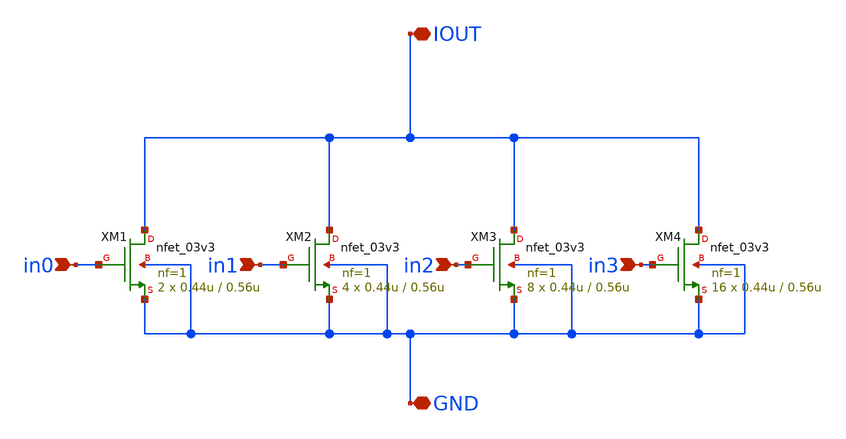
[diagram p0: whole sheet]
** sch_path: xschem/current_dac.sch
**.subckt current_dac in0 IOUT GND in1 in2 in3
*.ipin in0
*.iopin IOUT
*.iopin GND
*.ipin in1
*.ipin in2
*.ipin in3
XM1 IOUT in0 GND GND nfet_03v3 L=0.56u W=0.44u nf=1 ad='int((nf+1)/2) * W/nf * 0.18u' as='int((nf+2)/2) * W/nf * 0.18u'
+ pd='2*int((nf+1)/2) * (W/nf + 0.18u)' ps='2*int((nf+2)/2) * (W/nf + 0.18u)' nrd='0.18u / W' nrs='0.18u / W'
+ sa=0 sb=0 sd=0 m=2
XM2 IOUT in1 GND GND nfet_03v3 L=0.56u W=0.44u nf=1 ad='int((nf+1)/2) * W/nf * 0.18u' as='int((nf+2)/2) * W/nf * 0.18u'
+ pd='2*int((nf+1)/2) * (W/nf + 0.18u)' ps='2*int((nf+2)/2) * (W/nf + 0.18u)' nrd='0.18u / W' nrs='0.18u / W'
+ sa=0 sb=0 sd=0 m=4
XM3 IOUT in2 GND GND nfet_03v3 L=0.56u W=0.44u nf=1 ad='int((nf+1)/2) * W/nf * 0.18u' as='int((nf+2)/2) * W/nf * 0.18u'
+ pd='2*int((nf+1)/2) * (W/nf + 0.18u)' ps='2*int((nf+2)/2) * (W/nf + 0.18u)' nrd='0.18u / W' nrs='0.18u / W'
+ sa=0 sb=0 sd=0 m=8
XM4 IOUT in3 GND GND nfet_03v3 L=0.56u W=0.44u nf=1 ad='int((nf+1)/2) * W/nf * 0.18u' as='int((nf+2)/2) * W/nf * 0.18u'
+ pd='2*int((nf+1)/2) * (W/nf + 0.18u)' ps='2*int((nf+2)/2) * (W/nf + 0.18u)' nrd='0.18u / W' nrs='0.18u / W'
+ sa=0 sb=0 sd=0 m=16
**.ends
.end
